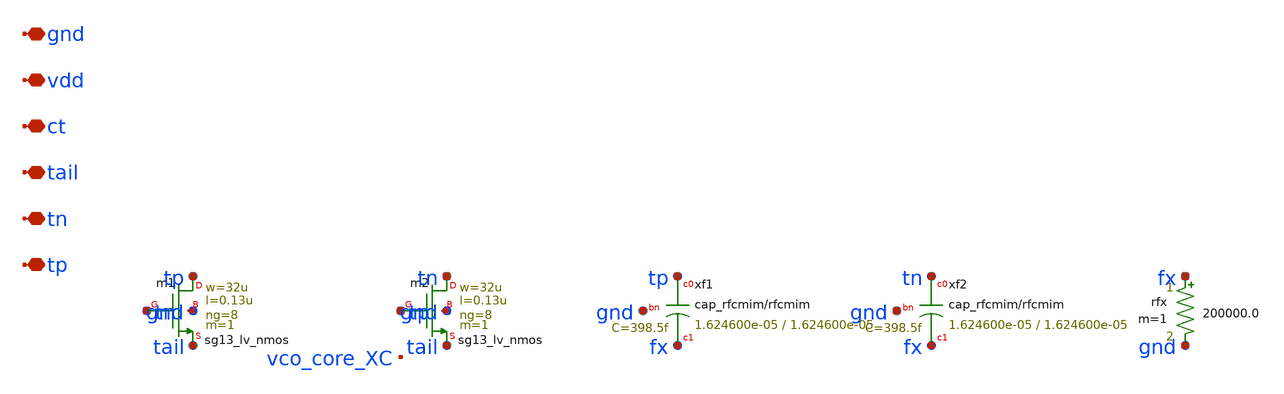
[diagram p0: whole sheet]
** sch_path: analog/vco/sch/vco_core.sch
**.subckt vco_core tp tn tail ct vdd gnd
*.iopin tp
*.iopin tn
*.iopin tail
*.iopin ct
*.iopin vdd
*.iopin gnd
Xm1 tp tn tail gnd sg13_lv_nmos w=32u l=0.13u ng=8 m=1 mm_ok=1
Xm2 tn tp tail gnd sg13_lv_nmos w=32u l=0.13u ng=8 m=1 mm_ok=1
Xxf1 tp fx gnd cap_rfcmim w=1.624600e-05 l=1.624600e-05 wfeed=5.0e-6 m=1 mm_ok=1
Xxf2 tn fx gnd cap_rfcmim w=1.624600e-05 l=1.624600e-05 wfeed=5.0e-6 m=1 mm_ok=1
rfx fx gnd 200000.0 m=1
**.ends
.end
